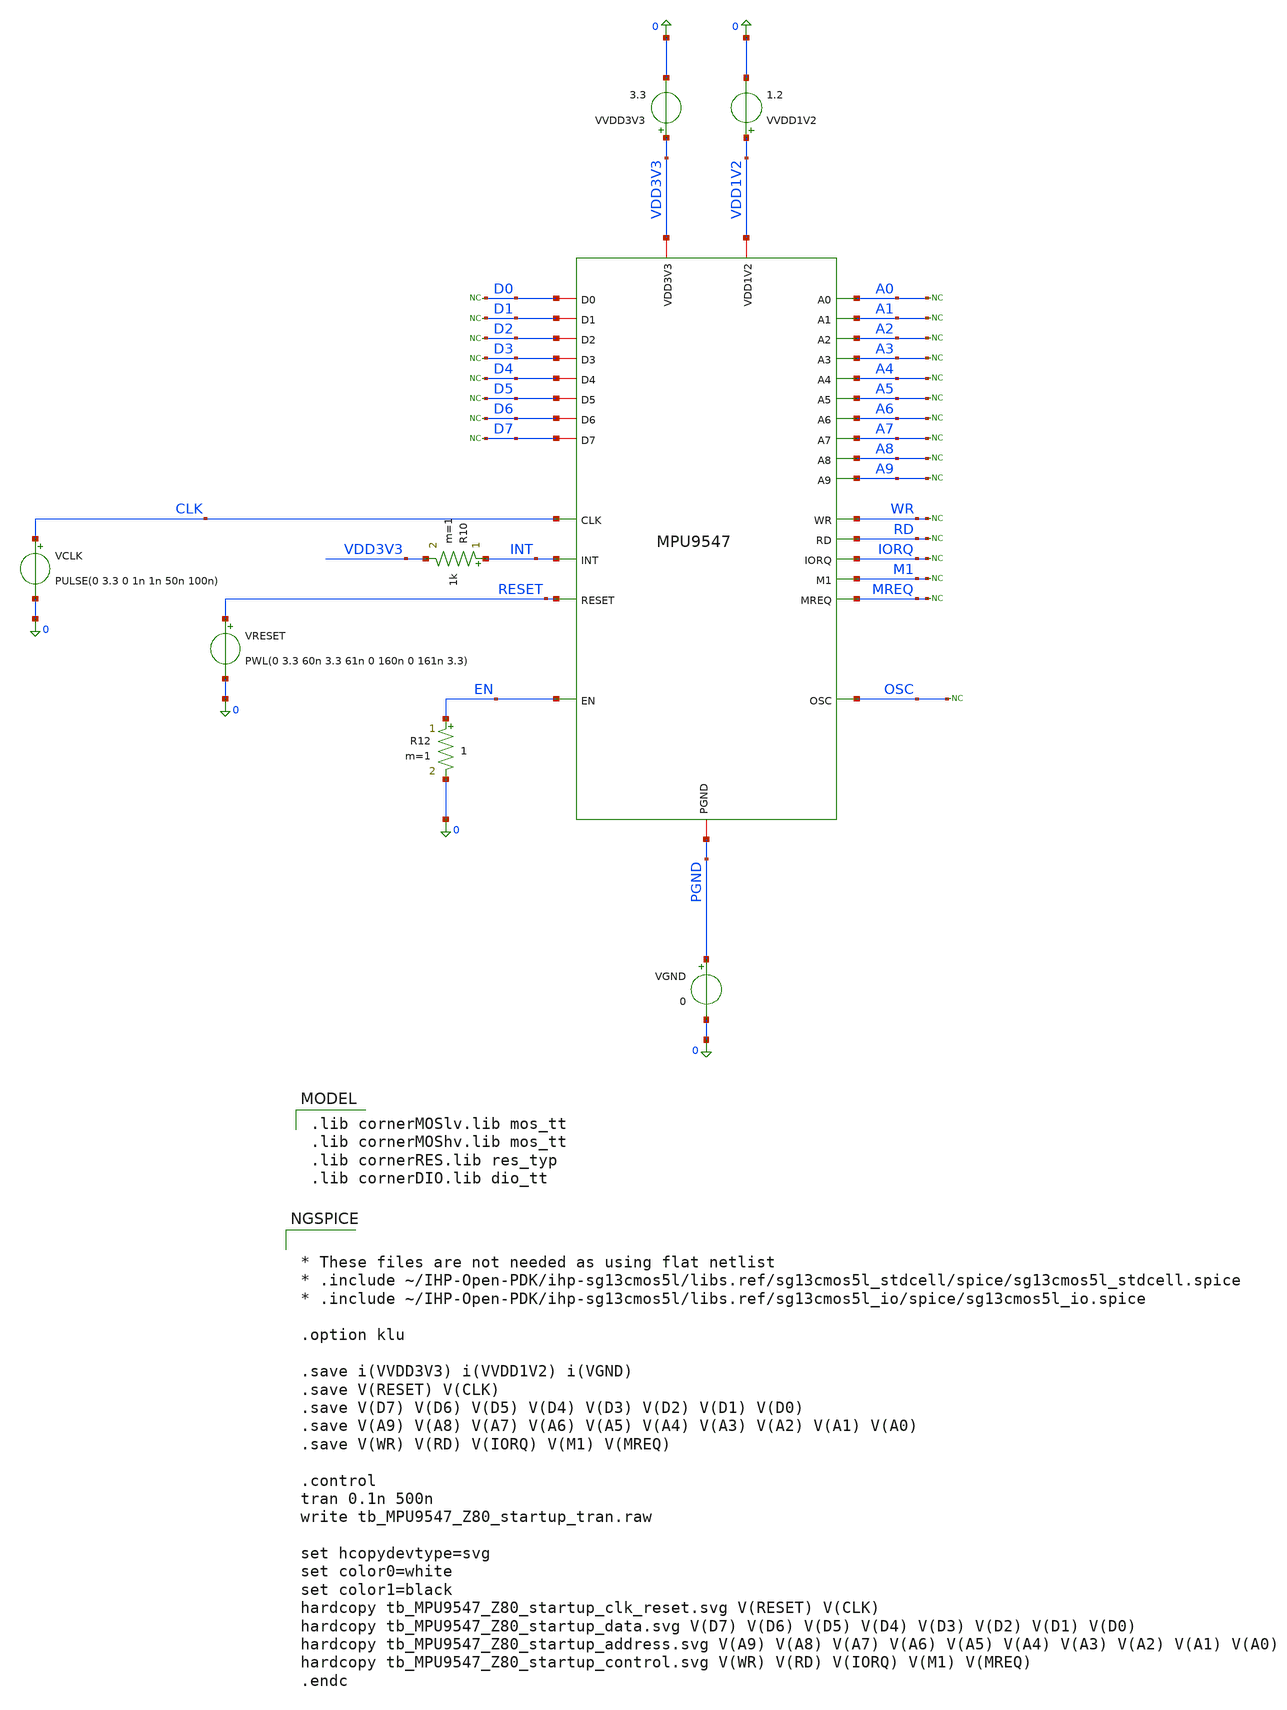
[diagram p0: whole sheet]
** sch_path: MPU9547-main/analog/schematic/tb_MPU9547_Z80_startup_tran.sch
**.subckt tb_MPU9547_Z80_startup_tran
VVDD3V3 VDD3V3 0 3.3
.save i(vvdd3v3)
VVDD1V2 VDD1V2 0 1.2
.save i(vvdd1v2)
* noconn A0
* noconn A1
* noconn A2
* noconn A3
* noconn A4
* noconn A5
* noconn A6
* noconn A7
* noconn A8
* noconn A9
* noconn WR
* noconn RD
* noconn IORQ
* noconn M1
* noconn MREQ
x1 A4 A5 A6 VDD3V3 PGND A7 A8 A9 IORQ M1 RESET OSC EN CLK INT MREQ WR RD D7 VDD1V2 D6 D5 D4 D3 D2 D1
+ D0 A0 A1 A2 A3 MPU9547
R10 INT VDD3V3 1k m=1
VGND PGND 0 0
.save i(vgnd)
R12 EN 0 1 m=1
* noconn OSC
* noconn D0
* noconn D1
* noconn D2
* noconn D3
* noconn D4
* noconn D5
* noconn D6
* noconn D7
VCLK CLK 0 PULSE(0 3.3 0 1n 1n 50n 100n)
VRESET RESET 0 PWL(0 3.3 60n 3.3 61n 0 160n 0 161n 3.3)
**** begin user architecture code
 .lib cornerMOSlv.lib mos_tt
.lib cornerMOShv.lib mos_tt
.lib cornerRES.lib res_typ
.lib cornerDIO.lib dio_tt



* These files are not needed as using flat netlist
* .include ~/IHP-Open-PDK/ihp-sg13cmos5l/libs.ref/sg13cmos5l_stdcell/spice/sg13cmos5l_stdcell.spice
* .include ~/IHP-Open-PDK/ihp-sg13cmos5l/libs.ref/sg13cmos5l_io/spice/sg13cmos5l_io.spice

.option klu

.save i(VVDD3V3) i(VVDD1V2) i(VGND)
.save V(RESET) V(CLK)
.save V(D7) V(D6) V(D5) V(D4) V(D3) V(D2) V(D1) V(D0)
.save V(A9) V(A8) V(A7) V(A6) V(A5) V(A4) V(A3) V(A2) V(A1) V(A0)
.save V(WR) V(RD) V(IORQ) V(M1) V(MREQ)

.control
tran 0.1n 500n
write tb_MPU9547_Z80_startup_tran.raw

set hcopydevtype=svg
set color0=white
set color1=black
hardcopy tb_MPU9547_Z80_startup_clk_reset.svg V(RESET) V(CLK)
hardcopy tb_MPU9547_Z80_startup_data.svg V(D7) V(D6) V(D5) V(D4) V(D3) V(D2) V(D1) V(D0)
hardcopy tb_MPU9547_Z80_startup_address.svg V(A9) V(A8) V(A7) V(A6) V(A5) V(A4) V(A3) V(A2) V(A1)
+ V(A0)
hardcopy tb_MPU9547_Z80_startup_control.svg V(WR) V(RD) V(IORQ) V(M1) V(MREQ)
.endc



**** end user architecture code
**.ends

* expanding   symbol:  MPU9547.sym # of pins=31
** sym_path: MPU9547-main/analog/schematic/MPU9547.sym
.include /home/lowneyd/projects/mandalore/analog/schematic/simulation/MPU9547_extracted.cir
.end
